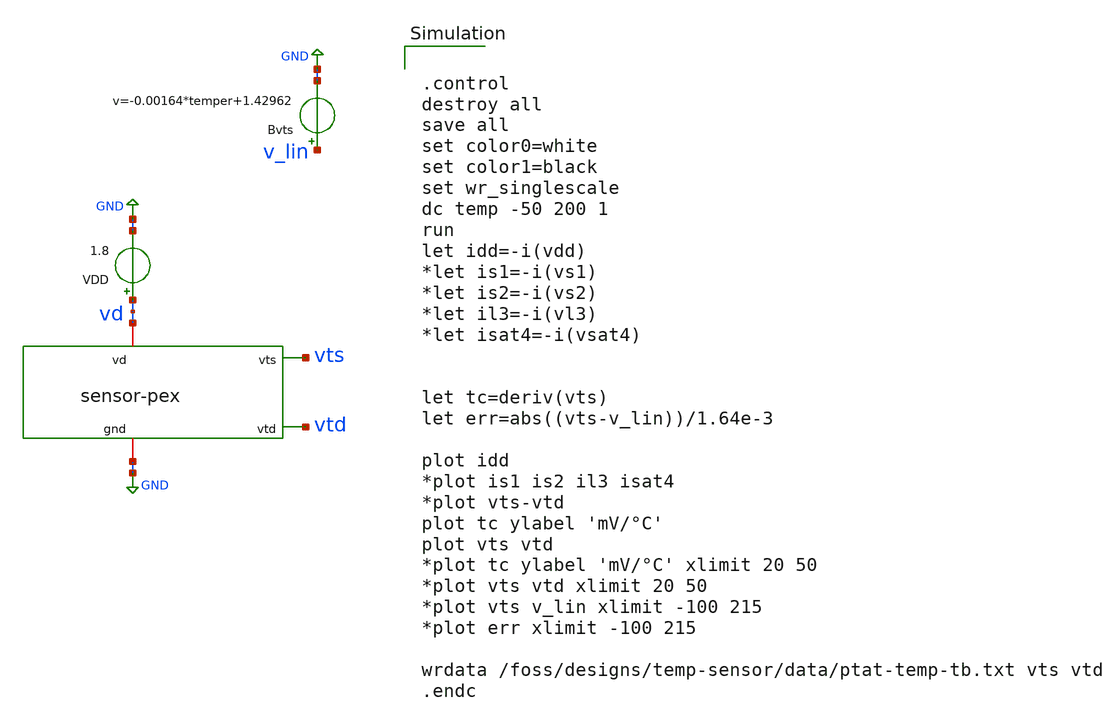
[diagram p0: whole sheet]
** sch_path: mag/sensor/xschem/tb-temp.sch
**.subckt tb-temp
VDD vd GND 1.8
Bvts v_lin GND v=-0.00164*temper+1.42962
x1 vd vts vtd GND sensor-pex
**** begin user architecture code


.control
destroy all
save all
set color0=white
set color1=black
set wr_singlescale
dc temp -50 200 1
run
let idd=-i(vdd)
*let is1=-i(vs1)
*let is2=-i(vs2)
*let il3=-i(vl3)
*let isat4=-i(vsat4)


let tc=deriv(vts)
let err=abs((vts-v_lin))/1.64e-3

plot idd
*plot is1 is2 il3 isat4
*plot vts-vtd
plot tc ylabel 'mV/°C'
plot vts vtd
*plot tc ylabel 'mV/°C' xlimit 20 50
*plot vts vtd xlimit 20 50
*plot vts v_lin xlimit -100 215
*plot err xlimit -100 215

wrdata /foss/designs/temp-sensor/data/ptat-temp-tb.txt vts vtd
.endc


 .lib $::SKYWATER_MODELS/sky130.lib.spice tt
.include $::SKYWATER_STDCELLS/sky130_fd_sc_hd.spice

**** end user architecture code
**.ends

* expanding   symbol:  /foss/designs/temp-sensor/sensor/xschem/sensor-pex.sym # of pins=4
** sym_path: mag/sensor/xschem/sensor-pex.sym
** sch_path: mag/sensor/xschem/sensor-pex.sch
.subckt sensor-pex vd vts vtd gnd
*.iopin vd
*.opin vts
*.opin vtd
*.iopin gnd
**** begin user architecture code



* NGSPICE file created from sensor.ext - technology: sky130A

*.subckt sensor vd vts vtd gnd
X0 b.t19 vtd c vd.t8 sky130_fd_pr__pfet_01v8 ad=0.29 pd=2.29 as=0.58 ps=4.58 w=2 l=1
X1 gnd b.t8 b gnd.t17 sky130_fd_pr__nfet_01v8 ad=0.29 pd=2.58 as=0.29 ps=2.58 w=1 l=1
X2 vtd b.t21 gnd.t40 gnd.t22 sky130_fd_pr__nfet_01v8 ad=0.29 pd=2.58 as=0.29 ps=2.58 w=1 l=1
X3 vtd b.t22 gnd.t39 gnd.t22 sky130_fd_pr__nfet_01v8 ad=0.29 pd=2.58 as=0.29 ps=2.58 w=1 l=1
X4 gnd.t68 gnd.t66 gnd.t67 gnd.t48 sky130_fd_pr__nfet_01v8 ad=0.29 pd=2.58 as=0 ps=0 w=1 l=1
X5 vts.t24 vtd.t12 vtd.t13 vts.t23 sky130_fd_pr__pfet_01v8 ad=0.29 pd=2.29 as=0.29 ps=2.29 w=2 l=1
X6 gnd.t38 b.t23 vtd gnd.t2 sky130_fd_pr__nfet_01v8 ad=0.29 pd=2.58 as=0.29 ps=2.58 w=1 l=1
X7 gnd.t37 b.t24 vtd gnd.t2 sky130_fd_pr__nfet_01v8 ad=0.29 pd=2.58 as=0.29 ps=2.58 w=1 l=1
X8 vts.t22 vtd.t16 vtd.t17 vts.t21 sky130_fd_pr__pfet_01v8 ad=0.29 pd=2.29 as=0.58 ps=4.58 w=2 l=1
X9 gnd b.t6 b gnd.t17 sky130_fd_pr__nfet_01v8 ad=0.29 pd=2.58 as=0.29 ps=2.58 w=1 l=1
X10 gnd b.t4 b gnd.t17 sky130_fd_pr__nfet_01v8 ad=0.29 pd=2.58 as=0.29 ps=2.58 w=1 l=1
X11 c vtd.t24 b.t18 vd.t7 sky130_fd_pr__pfet_01v8 ad=0.58 pd=4.58 as=0.29 ps=2.29 w=2 l=1
X12 vtd.t15 vtd.t14 vts.t20 vts.t19 sky130_fd_pr__pfet_01v8 ad=0.29 pd=2.29 as=0.29 ps=2.29 w=2 l=1
X13 gnd b.t27 a gnd.t10 sky130_fd_pr__nfet_01v8 ad=0.29 pd=2.58 as=0.29 ps=2.58 w=1 l=1
X14 d vtd.t25 vd.t6 vd.t5 sky130_fd_pr__pfet_01v8 ad=0.58 pd=4.58 as=0.58 ps=4.58 w=2 l=1
X15 c vtd.t26 b.t17 vd.t4 sky130_fd_pr__pfet_01v8 ad=0.29 pd=2.29 as=0.29 ps=2.29 w=2 l=1
X16 b b.t0 gnd.t30 gnd.t8 sky130_fd_pr__nfet_01v8 ad=0.29 pd=2.58 as=0.29 ps=2.58 w=1 l=1
X17 gnd.t65 gnd.t63 gnd.t64 gnd.t44 sky130_fd_pr__nfet_01v8 ad=0.29 pd=2.58 as=0 ps=0 w=1 l=1
X18 b b.t12 gnd.t29 gnd.t8 sky130_fd_pr__nfet_01v8 ad=0.29 pd=2.58 as=0.29 ps=2.58 w=1 l=1
X19 gnd.t62 gnd.t60 gnd.t61 gnd.t44 sky130_fd_pr__nfet_01v8 ad=0.29 pd=2.58 as=0 ps=0 w=1 l=1
X20 a a vd.t28 vd.t27 sky130_fd_pr__pfet_01v8 ad=0.58 pd=4.58 as=0.29 ps=2.29 w=2 l=1
X21 a b.t30 gnd gnd.t0 sky130_fd_pr__nfet_01v8 ad=0.29 pd=2.58 as=0.29 ps=2.58 w=1 l=1
X22 a b.t31 gnd gnd.t0 sky130_fd_pr__nfet_01v8 ad=0.29 pd=2.58 as=0.29 ps=2.58 w=1 l=1
X23 vd.t26 a a vd.t25 sky130_fd_pr__pfet_01v8 ad=0.29 pd=2.29 as=0.58 ps=4.58 w=2 l=1
X24 vtd b.t32 gnd.t24 gnd.t22 sky130_fd_pr__nfet_01v8 ad=0.29 pd=2.58 as=0.29 ps=2.58 w=1 l=1
X25 vts.t18 vtd.t20 vtd.t21 vts.t17 sky130_fd_pr__pfet_01v8 ad=0.29 pd=2.29 as=0.29 ps=2.29 w=2 l=1
X26 gnd.t59 gnd.t57 gnd.t58 gnd.t48 sky130_fd_pr__nfet_01v8 ad=0.29 pd=2.58 as=0 ps=0 w=1 l=1
X27 vd.t20 vd.t17 vd.t19 vd.t18 sky130_fd_pr__pfet_01v8 ad=0.58 pd=4.58 as=0 ps=0 w=2 l=1
X28 b.t16 vtd.t27 c vd.t3 sky130_fd_pr__pfet_01v8 ad=0.29 pd=2.29 as=0.29 ps=2.29 w=2 l=1
X29 vtd b.t33 gnd.t23 gnd.t22 sky130_fd_pr__nfet_01v8 ad=0.29 pd=2.58 as=0.29 ps=2.58 w=1 l=1
X30 gnd.t21 b.t34 vtd gnd.t2 sky130_fd_pr__nfet_01v8 ad=0.29 pd=2.58 as=0.29 ps=2.58 w=1 l=1
X31 gnd.t56 gnd.t54 gnd.t55 gnd.t48 sky130_fd_pr__nfet_01v8 ad=0.29 pd=2.58 as=0 ps=0 w=1 l=1
X32 c a d vd.t24 sky130_fd_pr__pfet_01v8 ad=0.58 pd=4.58 as=0.29 ps=2.29 w=2 l=1
X33 vtd.t19 vtd.t18 vts.t16 vts.t15 sky130_fd_pr__pfet_01v8 ad=0.29 pd=2.29 as=0.29 ps=2.29 w=2 l=1
X34 gnd.t53 gnd.t51 gnd.t52 gnd.t44 sky130_fd_pr__nfet_01v8 ad=0.29 pd=2.58 as=0 ps=0 w=1 l=1
X35 gnd.t50 gnd.t47 gnd.t49 gnd.t48 sky130_fd_pr__nfet_01v8 ad=0.29 pd=2.58 as=0 ps=0 w=1 l=1
X36 vd.t16 vd.t13 vd.t15 vd.t14 sky130_fd_pr__pfet_01v8 ad=0.58 pd=4.58 as=0 ps=0 w=2 l=1
X37 d a c vd.t23 sky130_fd_pr__pfet_01v8 ad=0.29 pd=2.29 as=0.29 ps=2.29 w=2 l=1
X38 b b.t14 gnd.t20 gnd.t8 sky130_fd_pr__nfet_01v8 ad=0.29 pd=2.58 as=0.29 ps=2.58 w=1 l=1
X39 gnd b.t2 b gnd.t17 sky130_fd_pr__nfet_01v8 ad=0.29 pd=2.58 as=0.29 ps=2.58 w=1 l=1
X40 vd.t12 vd.t9 vd.t11 vd.t10 sky130_fd_pr__pfet_01v8 ad=0.58 pd=4.58 as=0 ps=0 w=2 l=1
X41 c a d vd.t22 sky130_fd_pr__pfet_01v8 ad=0.29 pd=2.29 as=0.29 ps=2.29 w=2 l=1
X42 vtd.t11 vtd.t10 vts.t14 vts.t13 sky130_fd_pr__pfet_01v8 ad=0.29 pd=2.29 as=0.29 ps=2.29 w=2 l=1
X43 gnd b.t37 a gnd.t10 sky130_fd_pr__nfet_01v8 ad=0.29 pd=2.58 as=0.29 ps=2.58 w=1 l=1
X44 d a c vd.t21 sky130_fd_pr__pfet_01v8 ad=0.29 pd=2.29 as=0.58 ps=4.58 w=2 l=1
X45 gnd b.t38 a gnd.t10 sky130_fd_pr__nfet_01v8 ad=0.29 pd=2.58 as=0.29 ps=2.58 w=1 l=1
X46 gnd b.t39 a gnd.t10 sky130_fd_pr__nfet_01v8 ad=0.29 pd=2.58 as=0.29 ps=2.58 w=1 l=1
X47 b b.t10 gnd.t9 gnd.t8 sky130_fd_pr__nfet_01v8 ad=0.29 pd=2.58 as=0.29 ps=2.58 w=1 l=1
X48 gnd.t46 gnd.t43 gnd.t45 gnd.t44 sky130_fd_pr__nfet_01v8 ad=0.29 pd=2.58 as=0 ps=0 w=1 l=1
X49 gnd b.t41 vtd gnd.t2 sky130_fd_pr__nfet_01v8 ad=0.29 pd=2.58 as=0.29 ps=2.58 w=1 l=1
X50 a b.t42 gnd gnd.t0 sky130_fd_pr__nfet_01v8 ad=0.29 pd=2.58 as=0.29 ps=2.58 w=1 l=1
X51 vts.t7 vts.t4 vts.t6 vts.t5 sky130_fd_pr__pfet_01v8 ad=0.58 pd=4.58 as=0 ps=0 w=2 l=1
X52 vts.t12 vtd.t8 vtd.t9 vts.t11 sky130_fd_pr__pfet_01v8 ad=0.29 pd=2.29 as=0.29 ps=2.29 w=2 l=1
X53 vd.t2 vtd.t28 vts.t10 vd.t1 sky130_fd_pr__pfet_01v8 ad=0.58 pd=4.58 as=0.58 ps=4.58 w=2 l=5
X54 vtd.t23 vtd.t22 vts.t9 vts.t8 sky130_fd_pr__pfet_01v8 ad=0.58 pd=4.58 as=0.29 ps=2.29 w=2 l=1
X55 c c c vd.t0 sky130_fd_pr__pfet_01v8 ad=0.58 pd=4.58 as=4.64 ps=36.6 w=2 l=1
X56 vts.t3 vts.t0 vts.t2 vts.t1 sky130_fd_pr__pfet_01v8 ad=0.58 pd=4.58 as=0 ps=0 w=2 l=1
X57 a b.t43 gnd gnd.t0 sky130_fd_pr__nfet_01v8 ad=0.29 pd=2.58 as=0.29 ps=2.58 w=1 l=1
R0 vtd.n0 vtd.t25 64.6855
R1 vtd.n5 vtd.t24 64.3461
R2 vtd.n6 vtd.t26 63.6292
R3 vtd.n5 vtd.t27 63.6292
R4 vtd.n15 vtd.t16 63.6292
R5 vtd.n16 vtd.t10 63.6292
R6 vtd.n18 vtd.t20 63.6292
R7 vtd.n19 vtd.t14 63.6292
R8 vtd.n21 vtd.t8 63.6292
R9 vtd.n22 vtd.t18 63.6292
R10 vtd.n24 vtd.t12 63.6292
R11 vtd.n10 vtd.t22 63.6275
R12 vtd.n11 vtd.t23 14.3646
R13 vtd.n15 vtd.t17 14.3555
R14 vtd.n14 vtd.t21 14.283
R15 vtd.n14 vtd.t11 14.283
R16 vtd.n13 vtd.t9 14.283
R17 vtd.n13 vtd.t15 14.283
R18 vtd.n12 vtd.t13 14.283
R19 vtd.n12 vtd.t19 14.283
R20 vtd.n0 vtd.t28 13.7819
R21 vtd.n9 vtd.n8 4.52354
R22 vtd.n4 vtd.n3 4.5005
R23 vtd.n2 vtd.n1 4.5005
R24 vtd.n2 vtd.n0 3.05785
R25 vtd vtd.n27 1.29247
R26 vtd.n27 vtd.n26 0.981502
R27 vtd.n7 vtd.n6 0.792494
R28 vtd.n6 vtd.n5 0.717388
R29 vtd.n27 vtd.n9 0.41175
R30 vtd.n22 vtd.n21 0.134875
R31 vtd.n19 vtd.n18 0.134875
R32 vtd.n16 vtd.n15 0.134875
R33 vtd.n25 vtd.n24 0.0921667
R34 vtd.n24 vtd.n23 0.0676875
R35 vtd.n23 vtd.n22 0.0676875
R36 vtd.n21 vtd.n20 0.0676875
R37 vtd.n20 vtd.n19 0.0676875
R38 vtd.n18 vtd.n17 0.0676875
R39 vtd.n17 vtd.n16 0.0676875
R40 vtd.n11 vtd.n10 0.0516677
R41 vtd.n9 vtd.n4 0.03425
R42 vtd.n4 vtd.n2 0.0255
R43 vtd.n26 vtd.n25 0.022375
R44 vtd.n26 vtd.n11 0.0219082
R45 vtd.n8 vtd.n7 0.00963498
R46 vtd.n17 vtd.n14 0.00576717
R47 vtd.n20 vtd.n13 0.00576717
R48 vtd.n23 vtd.n12 0.00576717
R49 b.t10 b.t12 74.8549
R50 b.t0 b.t10 74.8549
R51 b.t14 b.t0 74.8549
R52 b.t2 b.t4 74.8549
R53 b.t6 b.t2 74.8549
R54 b.t8 b.t6 74.8549
R55 b.t33 b.t22 74.8549
R56 b.t21 b.t33 74.8549
R57 b.t32 b.t21 74.8549
R58 b.t34 b.t24 74.8549
R59 b.t23 b.t34 74.8549
R60 b.t41 b.t23 74.8549
R61 b.t42 b.t31 74.8549
R62 b.t30 b.t42 74.8549
R63 b.t43 b.t30 74.8549
R64 b.t27 b.t38 74.8549
R65 b.t39 b.t27 74.8549
R66 b.t37 b.t39 74.8549
R67 b.n3 b.t37 38.3763
R68 b.n7 b.t14 37.3622
R69 b.n6 b.t8 37.3602
R70 b.n5 b.t32 37.3602
R71 b.n4 b.t41 37.3602
R72 b.n3 b.t43 37.3602
R73 b.n0 b.t18 14.283
R74 b.n0 b.t16 14.283
R75 b.n1 b.t17 14.283
R76 b.n1 b.t19 14.283
R77 b b.n2 2.56613
R78 b b.n7 1.03722
R79 b.n7 b.n6 1.01707
R80 b.n4 b.n3 1.01657
R81 b.n5 b.n4 1.01657
R82 b.n6 b.n5 1.01657
R83 b.n2 b.n0 0.49917
R84 b.n2 b.n1 0.17267
R85 vd.n45 vd.n37 206.306
R86 vd.n17 vd.n14 168.66
R87 vd.t10 vd.n39 156.245
R88 vd.n5 vd.t7 143.697
R89 vd.n43 vd.t27 143.697
R90 vd.n45 vd.n42 126.871
R91 vd.n2 vd.n1 111.421
R92 vd.n15 vd.t4 86.6752
R93 vd.n7 vd.n4 85.0829
R94 vd.n26 vd.n21 79.0593
R95 vd.n27 vd.t14 71.8492
R96 vd.n5 vd.t18 65.0065
R97 vd.n9 vd.t17 63.6934
R98 vd.n32 vd.t13 63.6821
R99 vd.n49 vd.t9 63.6292
R100 vd.n29 vd.n26 63.2476
R101 vd.n15 vd.t8 60.4447
R102 vd.t4 vd.t1 58.1638
R103 vd.t14 vd.t22 58.1638
R104 vd.n24 vd.t5 42.1974
R105 vd.n35 vd.t21 42.1974
R106 vd.n12 vd.t3 28.5119
R107 vd.n40 vd.t10 21.0989
R108 vd.t5 vd.t24 19.3883
R109 vd.n27 vd.t23 17.1073
R110 vd.n31 vd.t6 14.5056
R111 vd.n8 vd.t2 14.472
R112 vd.n31 vd.t15 14.4415
R113 vd.n50 vd.t12 14.4388
R114 vd.n33 vd.t16 14.4153
R115 vd.n10 vd.t19 14.4127
R116 vd.n48 vd.t11 14.4041
R117 vd.n8 vd.t20 14.3878
R118 vd.n47 vd.t28 14.283
R119 vd.n47 vd.t26 14.283
R120 vd.t18 vd.t0 11.4051
R121 vd.n43 vd.t25 3.42187
R122 vd vd.n50 1.79592
R123 vd.n11 vd.n10 0.868662
R124 vd.n48 vd.n47 0.721906
R125 vd.n49 vd.n48 0.608294
R126 vd.n34 vd.n33 0.576317
R127 vd.n18 vd.n11 0.5755
R128 vd.n30 vd.n18 0.488
R129 vd.n46 vd.n34 0.463
R130 vd.n33 vd.n32 0.344245
R131 vd vd.n46 0.2755
R132 vd.n34 vd.n30 0.238
R133 vd.n9 vd.n8 0.129979
R134 vd.n50 vd.n49 0.100468
R135 vd.n32 vd.n31 0.0321654
R136 vd.n4 vd.n3 0.0307238
R137 vd.n3 vd.n2 0.0302348
R138 vd.n10 vd.n9 0.0267443
R139 vd.n42 vd.n41 0.0175052
R140 vd.n41 vd.n40 0.0175052
R141 vd.n21 vd.n20 0.0150968
R142 vd.n20 vd.n19 0.0150968
R143 vd.n14 vd.n13 0.0122827
R144 vd.n13 vd.n12 0.0122827
R145 vd.n37 vd.n36 0.00973799
R146 vd.n36 vd.n35 0.00973799
R147 vd.n17 vd.n16 0.00391284
R148 vd.n16 vd.n15 0.00391284
R149 vd.n29 vd.n28 0.00391284
R150 vd.n28 vd.n27 0.00391284
R151 vd.n45 vd.n44 0.00391284
R152 vd.n44 vd.n43 0.00391284
R153 vd.n7 vd.n6 0.00391284
R154 vd.n6 vd.n5 0.00391284
R155 vd.n39 vd.n38 0.00347027
R156 vd.n1 vd.n0 0.00347027
R157 vd.n26 vd.n25 0.00275116
R158 vd.n25 vd.n24 0.00275116
R159 vd.n24 vd.n23 0.00162558
R160 vd.n23 vd.n22 0.00162558
R161 vd.n18 vd.n17 0.000532663
R162 vd.n30 vd.n29 0.000532663
R163 vd.n46 vd.n45 0.000532663
R164 vd.n11 vd.n7 0.000532663
R165 gnd.n6 gnd.t8 709.494
R166 gnd.n119 gnd.t10 701.865
R167 gnd.t17 gnd.n27 633.203
R168 gnd.n26 gnd.n25 585
R169 gnd.n111 gnd.n110 585
R170 gnd.n116 gnd.n115 585
R171 gnd.n4 gnd.n3 585
R172 gnd.n76 gnd.t2 472.995
R173 gnd.n4 gnd.n2 398.683
R174 gnd.n116 gnd.n114 381.365
R175 gnd.t44 gnd.n5 366.19
R176 gnd.n34 gnd.t22 270.829
R177 gnd.t48 gnd.n118 270.829
R178 gnd.n76 gnd.t0 251.756
R179 gnd.n28 gnd.t17 167.838
R180 gnd.n78 gnd.n75 163.766
R181 gnd.n121 gnd.n111 156.236
R182 gnd.n37 gnd.n36 153.976
R183 gnd.n35 gnd.n30 150.648
R184 gnd.n37 gnd.n26 148.707
R185 gnd.t10 gnd.n117 137.321
R186 gnd.n8 gnd.n4 65.8829
R187 gnd.n113 gnd.n112 57.226
R188 gnd.n34 gnd.n31 49.5887
R189 gnd.n121 gnd.n116 48.5652
R190 gnd.n103 gnd.t47 37.3602
R191 gnd.n106 gnd.t66 37.3602
R192 gnd.n109 gnd.t54 37.3602
R193 gnd.n13 gnd.t63 37.3602
R194 gnd.n16 gnd.t43 37.3602
R195 gnd.n19 gnd.t60 37.3602
R196 gnd.n119 gnd.t48 22.8874
R197 gnd.n10 gnd.t51 18.6812
R198 gnd.n100 gnd.t57 18.6809
R199 gnd.n50 gnd.t24 17.8538
R200 gnd.n21 gnd.t20 17.7911
R201 gnd.n23 gnd.t29 17.4386
R202 gnd.n22 gnd.t9 17.4307
R203 gnd.n21 gnd.t30 17.4235
R204 gnd.n99 gnd.t59 17.405
R205 gnd.n99 gnd.t58 17.405
R206 gnd.n102 gnd.t50 17.405
R207 gnd.n102 gnd.t49 17.405
R208 gnd.n105 gnd.t68 17.405
R209 gnd.n105 gnd.t67 17.405
R210 gnd.n108 gnd.t56 17.405
R211 gnd.n108 gnd.t55 17.405
R212 gnd.n9 gnd.t53 17.405
R213 gnd.n9 gnd.t52 17.405
R214 gnd.n12 gnd.t65 17.405
R215 gnd.n12 gnd.t64 17.405
R216 gnd.n15 gnd.t46 17.405
R217 gnd.n15 gnd.t45 17.405
R218 gnd.n18 gnd.t62 17.405
R219 gnd.n18 gnd.t61 17.405
R220 gnd.n40 gnd.t38 17.4034
R221 gnd.n44 gnd.t40 17.4034
R222 gnd.n52 gnd.t21 17.4034
R223 gnd.n56 gnd.t23 17.4034
R224 gnd.n64 gnd.t37 17.4034
R225 gnd.n67 gnd.t39 17.4034
R226 gnd.n6 gnd.t44 15.2584
R227 gnd.n8 gnd.n7 9.3005
R228 gnd.n7 gnd.n6 9.3005
R229 gnd.n37 gnd.n29 9.3005
R230 gnd.n29 gnd.n28 9.3005
R231 gnd.n78 gnd.n77 9.3005
R232 gnd.n77 gnd.n76 9.3005
R233 gnd.n121 gnd.n120 9.3005
R234 gnd.n120 gnd.n119 9.3005
R235 gnd.n67 gnd.n66 6.38136
R236 gnd.n56 gnd.n55 5.4504
R237 gnd.n64 gnd.n63 5.3168
R238 gnd.n44 gnd.n43 4.92428
R239 gnd.n52 gnd.n51 4.41733
R240 gnd.n40 gnd.n39 3.98894
R241 gnd.n98 gnd.n97 0.624475
R242 gnd.n62 gnd.n50 0.438
R243 gnd.n73 gnd.n62 0.438
R244 gnd.n74 gnd.n73 0.375501
R245 gnd.n22 gnd.n21 0.3755
R246 gnd.n23 gnd.n22 0.3755
R247 gnd.n24 gnd.n23 0.330858
R248 gnd.n24 gnd.n20 0.290469
R249 gnd.n90 gnd.n87 0.287084
R250 gnd.n74 gnd.n38 0.281539
R251 gnd.n89 gnd.n88 0.278696
R252 gnd.n81 gnd.n80 0.278696
R253 gnd.n79 gnd.n74 0.245825
R254 gnd.n123 gnd.n98 0.244548
R255 gnd.n98 gnd.n79 0.180349
R256 gnd.n38 gnd.n24 0.156539
R257 gnd.n94 gnd.n91 0.143628
R258 gnd.n85 gnd.n82 0.143628
R259 gnd.n86 gnd.n85 0.128841
R260 gnd.n49 gnd.n48 0.128341
R261 gnd.n61 gnd.n60 0.128341
R262 gnd.n72 gnd.n71 0.128341
R263 gnd.n95 gnd.n94 0.1255
R264 gnd.n87 gnd.n86 0.0831431
R265 gnd.n97 gnd.n96 0.08175
R266 gnd.n101 gnd.n100 0.073412
R267 gnd.n11 gnd.n10 0.0734113
R268 gnd.n12 gnd.n11 0.0610469
R269 gnd.n13 gnd.n12 0.0610469
R270 gnd.n15 gnd.n14 0.0610469
R271 gnd.n16 gnd.n15 0.0610469
R272 gnd.n18 gnd.n17 0.0610469
R273 gnd.n19 gnd.n18 0.0610469
R274 gnd.n102 gnd.n101 0.0610469
R275 gnd.n103 gnd.n102 0.0610469
R276 gnd.n105 gnd.n104 0.0610469
R277 gnd.n106 gnd.n105 0.0610469
R278 gnd.n108 gnd.n107 0.0610469
R279 gnd.n109 gnd.n108 0.0610469
R280 gnd.n122 gnd.n109 0.0573558
R281 gnd.n20 gnd.n19 0.0573547
R282 gnd.n72 gnd.n68 0.05725
R283 gnd.n72 gnd.n65 0.05725
R284 gnd.n61 gnd.n57 0.051
R285 gnd.n61 gnd.n53 0.051
R286 gnd.n123 gnd.n122 0.0464211
R287 gnd.n49 gnd.n41 0.04475
R288 gnd.n49 gnd.n45 0.04475
R289 gnd.n14 gnd.n13 0.0426875
R290 gnd.n17 gnd.n16 0.0426875
R291 gnd.n104 gnd.n103 0.0426875
R292 gnd.n107 gnd.n106 0.0426875
R293 gnd gnd.n123 0.0415156
R294 gnd.n10 gnd.n9 0.031274
R295 gnd.n100 gnd.n99 0.0312734
R296 gnd.n68 gnd.n67 0.0144748
R297 gnd.n57 gnd.n56 0.0136712
R298 gnd.n48 gnd.n46 0.013
R299 gnd.n48 gnd.n47 0.013
R300 gnd.n45 gnd.n44 0.0127783
R301 gnd.n60 gnd.n58 0.009875
R302 gnd.n60 gnd.n59 0.009875
R303 gnd.n36 gnd.n35 0.0092427
R304 gnd.n35 gnd.n34 0.0092427
R305 gnd.n93 gnd.n92 0.00902273
R306 gnd.n84 gnd.n83 0.00902273
R307 gnd.n114 gnd.n113 0.00883856
R308 gnd.n2 gnd.n1 0.00883856
R309 gnd.n1 gnd.n0 0.00883856
R310 gnd.n65 gnd.n64 0.00867119
R311 gnd.n53 gnd.n52 0.00831404
R312 gnd.n41 gnd.n40 0.00791722
R313 gnd.n71 gnd.n69 0.00675
R314 gnd.n71 gnd.n70 0.00675
R315 gnd.n96 gnd.n90 0.00635717
R316 gnd.n33 gnd.n32 0.00487141
R317 gnd.n34 gnd.n33 0.00487141
R318 gnd.n94 gnd.n93 0.00476136
R319 gnd.n49 gnd.n42 0.00409445
R320 gnd.n61 gnd.n54 0.00393561
R321 gnd.n86 gnd.n81 0.00353363
R322 gnd.n85 gnd.n84 0.00334091
R323 gnd.n122 gnd.n121 0.00152216
R324 gnd.n20 gnd.n8 0.00152195
R325 gnd.n90 gnd.n89 0.00100166
R326 gnd.n38 gnd.n37 0.000522345
R327 gnd.n79 gnd.n78 0.000522345
R328 gnd.n73 gnd.n72 0.000501021
R329 gnd.n62 gnd.n61 0.000501021
R330 gnd.n50 gnd.n49 0.000501021
R331 gnd.n96 gnd.n95 0.000500579
R332 vts.n22 vts.n17 761.601
R333 vts.n23 vts.n22 641.883
R334 vts.t1 vts.t8 333.303
R335 vts.n16 vts.t5 262.014
R336 vts.n26 vts.t1 237.054
R337 vts.t8 vts.t23 229.925
R338 vts.t11 vts.t15 229.925
R339 vts.t19 vts.t17 229.925
R340 vts.t17 vts.t13 229.925
R341 vts.t13 vts.t21 229.925
R342 vts.n20 vts.t11 130.113
R343 vts.n20 vts.t19 99.8129
R344 vts.n11 vts.t0 63.6292
R345 vts.n4 vts.t4 63.6292
R346 vts.n30 vts.n29 37.8314
R347 vts.n12 vts.t10 16.8006
R348 vts.n5 vts.t6 14.4639
R349 vts.n10 vts.t3 14.4362
R350 vts.n13 vts.t2 14.4313
R351 vts.n4 vts.t7 14.3697
R352 vts.n0 vts.t9 14.283
R353 vts.n0 vts.t24 14.283
R354 vts.n1 vts.t16 14.283
R355 vts.n1 vts.t12 14.283
R356 vts.n2 vts.t20 14.283
R357 vts.n2 vts.t18 14.283
R358 vts.n3 vts.t14 14.283
R359 vts.n3 vts.t22 14.283
R360 vts vts.n32 0.88175
R361 vts.n9 vts.n8 0.6455
R362 vts.n8 vts.n7 0.6455
R363 vts.n7 vts.n6 0.6455
R364 vts.n6 vts.n5 0.450361
R365 vts.n10 vts.n9 0.440551
R366 vts.n31 vts.n30 0.369912
R367 vts.n5 vts.n4 0.0741592
R368 vts.n11 vts.n10 0.0682354
R369 vts.n13 vts.n11 0.0634447
R370 vts.n25 vts.n24 0.0431282
R371 vts.n24 vts.n23 0.0426316
R372 vts.n32 vts.n31 0.0305459
R373 vts.n27 vts.n15 0.0180045
R374 vts.n15 vts.n14 0.0175052
R375 vts.n9 vts.n0 0.0129196
R376 vts.n8 vts.n1 0.0129196
R377 vts.n7 vts.n2 0.0129196
R378 vts.n6 vts.n3 0.0129196
R379 vts.n28 vts.n27 0.0111828
R380 vts.n29 vts.n28 0.0106833
R381 vts.n17 vts.n16 0.00559165
R382 vts.n22 vts.n21 0.00192573
R383 vts.n21 vts.n20 0.00192573
R384 vts.n19 vts.n18 0.00192573
R385 vts.n20 vts.n19 0.00192573
R386 vts.n31 vts.n13 0.00106714
R387 vts.n26 vts.n25 0.00100046
R388 vts.n27 vts.n26 0.00100029
R389 vts.n13 vts.n12 0.000503978
C0 a vts 0.543f
C1 vts b 0.972f
C2 vtd vd 3.41f
C3 a c 0.997f
C4 c b 0.55f
C5 vts d 0.248f
C6 a b 0.821f
C7 c d 0.492f
C8 a d 0.588f
C9 d b 0.0152f
C10 vts vd 0.494f
C11 c vd 0.787f
C12 vts vtd 7.5f
C13 c vtd 1.12f
C14 a vd 2.92f
C15 b vd 0.0693f
C16 a vtd 2.14f
C17 vtd b 4.55f
C18 d vd 0.282f
C19 d vtd 0.3f
C20 vts c 0.166f
*.ends



**** end user architecture code
.ends

.GLOBAL GND
.end
